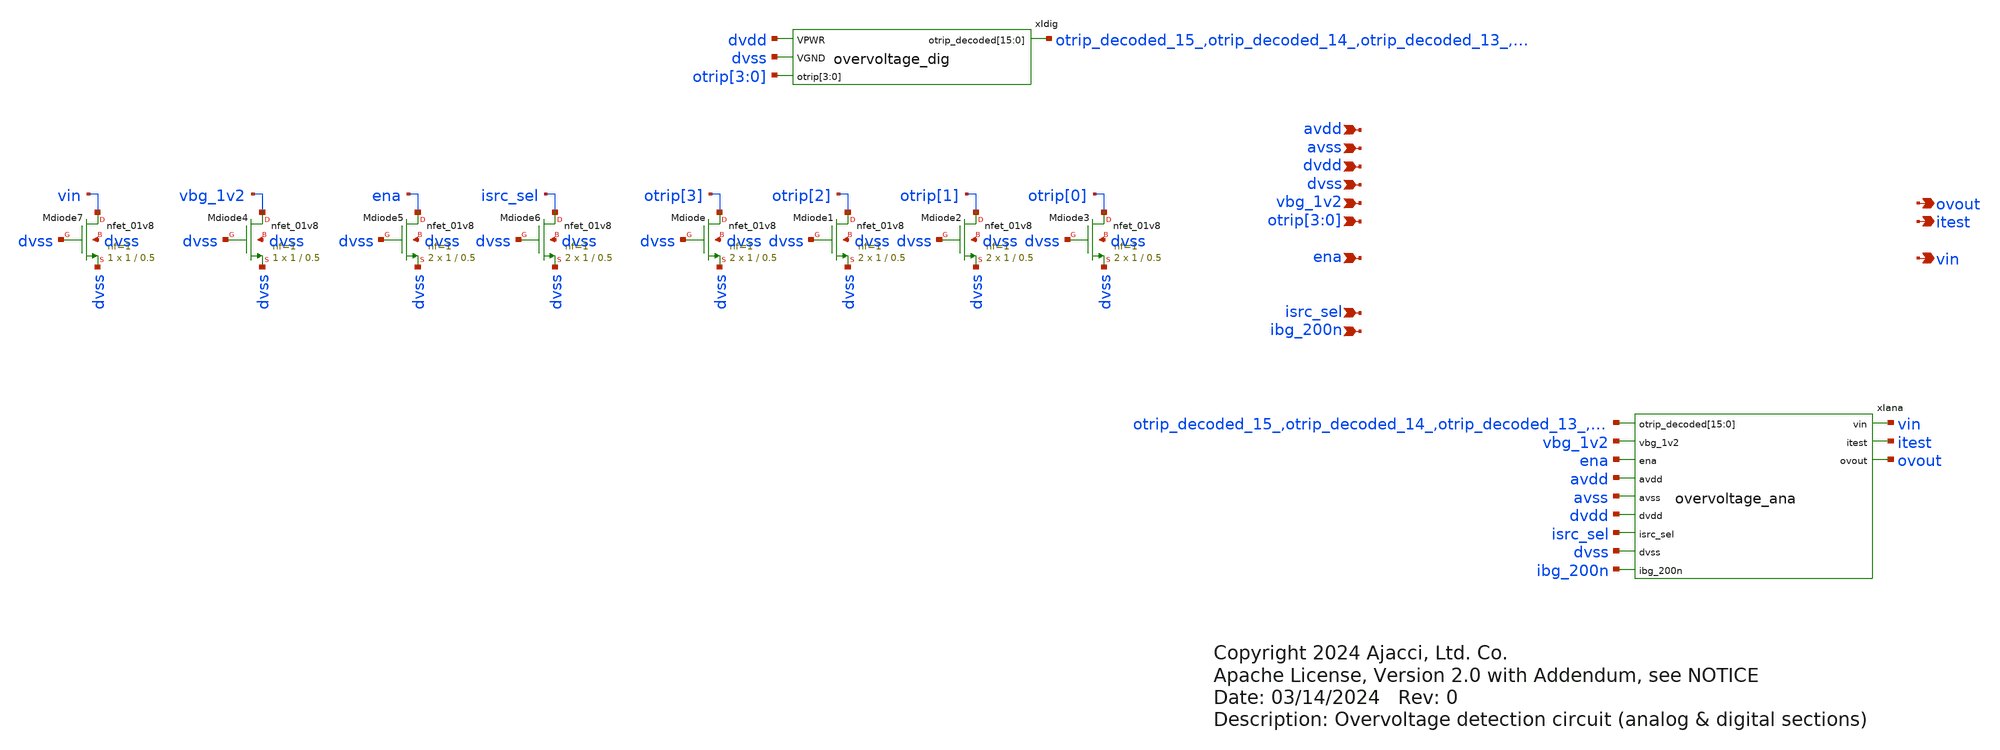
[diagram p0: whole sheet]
** sch_path: xschem/sky130_ajc_ip__overvoltage.sch
* Copyright 2024 Ajacci, Ltd. Co.
* Apache License, Version 2.0 with Addendum, see NOTICE
**.subckt sky130_ajc_ip__overvoltage avdd avss dvdd dvss vbg_1v2 otrip[3],otrip[2],otrip[1],otrip[0]
*+ ena isrc_sel ibg_200n vin ovout itest
*.ipin avdd
*.ipin avss
*.ipin dvdd
*.ipin dvss
*.ipin vbg_1v2
*.ipin otrip[3],otrip[2],otrip[1],otrip[0]
*.ipin ena
*.ipin isrc_sel
*.ipin ibg_200n
*.opin vin
*.opin ovout
*.opin itest
xIana otrip_decoded_15_ otrip_decoded_14_ otrip_decoded_13_ otrip_decoded_12_ otrip_decoded_11_
+ otrip_decoded_10_ otrip_decoded_9_ otrip_decoded_8_ otrip_decoded_7_ otrip_decoded_6_ otrip_decoded_5_
+ otrip_decoded_4_ otrip_decoded_3_ otrip_decoded_2_ otrip_decoded_1_ otrip_decoded_0_ vbg_1v2 ena avdd avss dvdd
+ isrc_sel dvss vin itest ibg_200n ovout overvoltage_ana
xIdig dvdd otrip_decoded_15_ otrip_decoded_14_ otrip_decoded_13_ otrip_decoded_12_ otrip_decoded_11_
+ otrip_decoded_10_ otrip_decoded_9_ otrip_decoded_8_ otrip_decoded_7_ otrip_decoded_6_ otrip_decoded_5_
+ otrip_decoded_4_ otrip_decoded_3_ otrip_decoded_2_ otrip_decoded_1_ otrip_decoded_0_ dvss otrip[3] otrip[2] otrip[1]
+ otrip[0] overvoltage_dig
XMdiode otrip[3] dvss dvss dvss sky130_fd_pr__nfet_01v8 L=0.5 W=1 nf=1 ad='int((nf+1)/2) * W/nf * 0.29'
+ as='int((nf+2)/2) * W/nf * 0.29' pd='2*int((nf+1)/2) * (W/nf + 0.29)' ps='2*int((nf+2)/2) * (W/nf + 0.29)'
+ nrd='0.29 / W' nrs='0.29 / W' sa=0 sb=0 sd=0 mult=2 m=2
XMdiode1 otrip[2] dvss dvss dvss sky130_fd_pr__nfet_01v8 L=0.5 W=1 nf=1 ad='int((nf+1)/2) * W/nf * 0.29'
+ as='int((nf+2)/2) * W/nf * 0.29' pd='2*int((nf+1)/2) * (W/nf + 0.29)' ps='2*int((nf+2)/2) * (W/nf + 0.29)'
+ nrd='0.29 / W' nrs='0.29 / W' sa=0 sb=0 sd=0 mult=2 m=2
XMdiode2 otrip[1] dvss dvss dvss sky130_fd_pr__nfet_01v8 L=0.5 W=1 nf=1 ad='int((nf+1)/2) * W/nf * 0.29'
+ as='int((nf+2)/2) * W/nf * 0.29' pd='2*int((nf+1)/2) * (W/nf + 0.29)' ps='2*int((nf+2)/2) * (W/nf + 0.29)'
+ nrd='0.29 / W' nrs='0.29 / W' sa=0 sb=0 sd=0 mult=2 m=2
XMdiode3 otrip[0] dvss dvss dvss sky130_fd_pr__nfet_01v8 L=0.5 W=1 nf=1 ad='int((nf+1)/2) * W/nf * 0.29'
+ as='int((nf+2)/2) * W/nf * 0.29' pd='2*int((nf+1)/2) * (W/nf + 0.29)' ps='2*int((nf+2)/2) * (W/nf + 0.29)'
+ nrd='0.29 / W' nrs='0.29 / W' sa=0 sb=0 sd=0 mult=2 m=2
XMdiode4 vbg_1v2 dvss dvss dvss sky130_fd_pr__nfet_01v8 L=0.5 W=1 nf=1 ad='int((nf+1)/2) * W/nf * 0.29'
+ as='int((nf+2)/2) * W/nf * 0.29' pd='2*int((nf+1)/2) * (W/nf + 0.29)' ps='2*int((nf+2)/2) * (W/nf + 0.29)'
+ nrd='0.29 / W' nrs='0.29 / W' sa=0 sb=0 sd=0 mult=1 m=1
XMdiode5 ena dvss dvss dvss sky130_fd_pr__nfet_01v8 L=0.5 W=1 nf=1 ad='int((nf+1)/2) * W/nf * 0.29' as='int((nf+2)/2) * W/nf * 0.29'
+ pd='2*int((nf+1)/2) * (W/nf + 0.29)' ps='2*int((nf+2)/2) * (W/nf + 0.29)' nrd='0.29 / W' nrs='0.29 / W'
+ sa=0 sb=0 sd=0 mult=2 m=2
XMdiode6 isrc_sel dvss dvss dvss sky130_fd_pr__nfet_01v8 L=0.5 W=1 nf=1 ad='int((nf+1)/2) * W/nf * 0.29'
+ as='int((nf+2)/2) * W/nf * 0.29' pd='2*int((nf+1)/2) * (W/nf + 0.29)' ps='2*int((nf+2)/2) * (W/nf + 0.29)'
+ nrd='0.29 / W' nrs='0.29 / W' sa=0 sb=0 sd=0 mult=2 m=2
XMdiode7 vin dvss dvss dvss sky130_fd_pr__nfet_01v8 L=0.5 W=1 nf=1 ad='int((nf+1)/2) * W/nf * 0.29' as='int((nf+2)/2) * W/nf * 0.29'
+ pd='2*int((nf+1)/2) * (W/nf + 0.29)' ps='2*int((nf+2)/2) * (W/nf + 0.29)' nrd='0.29 / W' nrs='0.29 / W'
+ sa=0 sb=0 sd=0 mult=1 m=1
**.ends
.end
